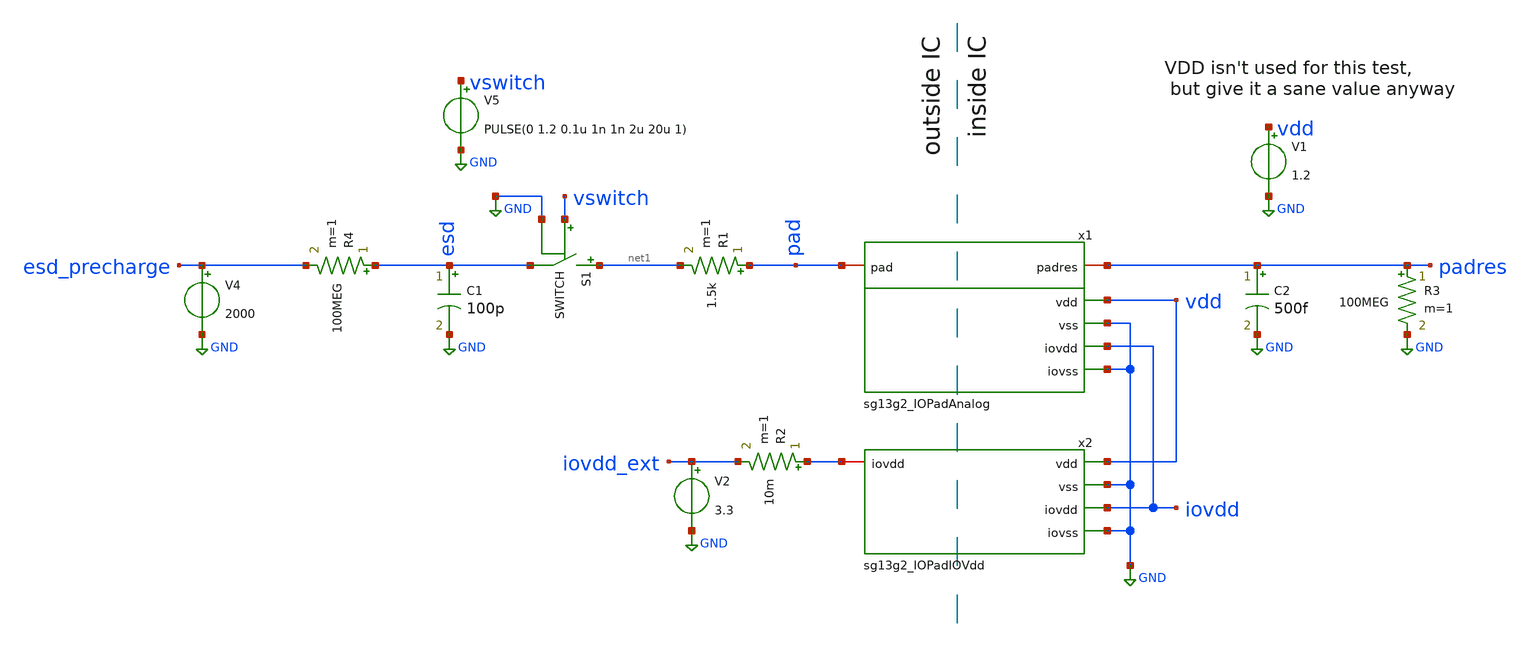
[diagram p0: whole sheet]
** sch_path: xschem/esd_test_iopadanalog.sch
**.subckt esd_test_iopadanalog
C1 esd GND 100p m=1
R1 pad net1 1.5k m=1
x1 GND vdd GND iovdd pad padres sg13g2_IOPadAnalog
V1 vdd GND 1.2
C2 padres GND 500f m=1
S1 net1 esd vswitch GND SWITCH
x2 GND vdd GND iovdd sg13g2_IOPadIOVdd
V2 iovdd_ext GND 3.3
R2 iovdd iovdd_ext 10m m=1
R3 padres GND 100MEG m=1
V4 esd_precharge GND 2000
V5 vswitch GND PULSE(0 1.2 0.1u 1n 1n 2u 20u 1)
R4 esd esd_precharge 100MEG m=1
**** begin user architecture code



** IHP models
.lib cornerMOSlv.lib mos_tt
.lib cornerMOShv.lib mos_tt
.lib cornerHBT.lib hbt_typ
.lib cornerRES.lib res_typ
.lib cornerCAP.lib cap_typ
.include diodes.lib

.include sg13g2_stdcell.spice
.include sg13g2_io.spi

* IHP's IO library uses sub! for implicit substrate connections...
.global sub!
vsub gnd sub! 0

* Switch model
.MODEL SWITCH SW   VT=0.9 VH=0.01  RON=0.01 ROFF=10G




.option chgtol=1e-11
.option method=gear
.save all
.probe i(c1)
.control
  set nostepsizelimit
  tran 0.1n 2u
  write esd_test_iopadanalog.raw

  rusage
  *quit
.endc









**** end user architecture code
**.ends
.GLOBAL GND
.end
